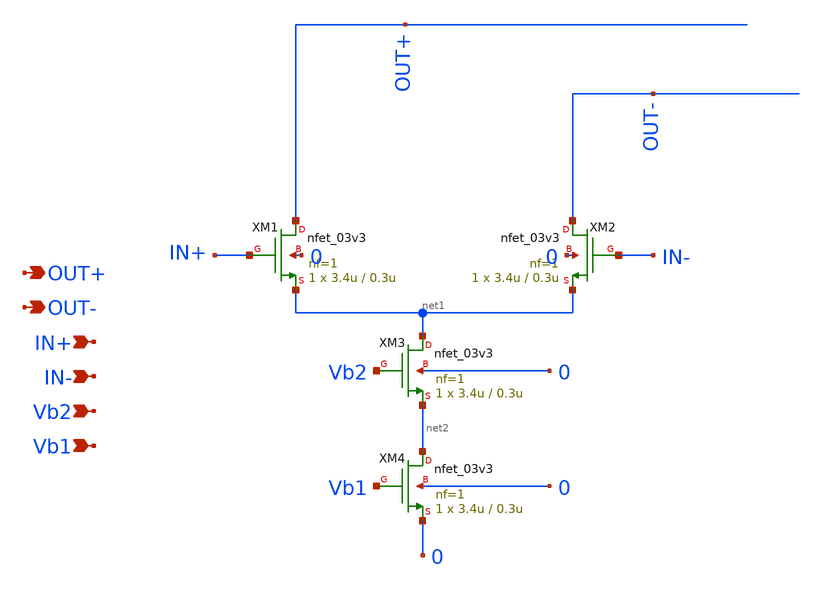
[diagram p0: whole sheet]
** sch_path: initial_notebooks_2023/accepted_notebooks/Current-Steering-DAC/DAC/current_unitx4.sch
**.subckt current_unitx4 IN+ IN- Vb2 Vb1 OUT+ OUT-
*.ipin IN+
*.ipin IN-
*.ipin Vb2
*.ipin Vb1
*.opin OUT+
*.opin OUT-
XM1 OUT+ IN+ net1 0 nfet_03v3 L=0.3u W=3.4u nf=1 ad='int((nf+1)/2) * W/nf * 0.18u' as='int((nf+2)/2) * W/nf * 0.18u'
+ pd='2*int((nf+1)/2) * (W/nf + 0.18u)' ps='2*int((nf+2)/2) * (W/nf + 0.18u)' nrd='0.18u / W' nrs='0.18u / W'
+ sa=0 sb=0 sd=0 m=1
XM2 OUT- IN- net1 0 nfet_03v3 L=0.3u W=3.4u nf=1 ad='int((nf+1)/2) * W/nf * 0.18u' as='int((nf+2)/2) * W/nf * 0.18u'
+ pd='2*int((nf+1)/2) * (W/nf + 0.18u)' ps='2*int((nf+2)/2) * (W/nf + 0.18u)' nrd='0.18u / W' nrs='0.18u / W'
+ sa=0 sb=0 sd=0 m=1
XM3 net1 Vb2 net2 0 nfet_03v3 L=0.3u W=3.4u nf=1 ad='int((nf+1)/2) * W/nf * 0.18u' as='int((nf+2)/2) * W/nf * 0.18u'
+ pd='2*int((nf+1)/2) * (W/nf + 0.18u)' ps='2*int((nf+2)/2) * (W/nf + 0.18u)' nrd='0.18u / W' nrs='0.18u / W'
+ sa=0 sb=0 sd=0 m=1
XM4 net2 Vb1 0 0 nfet_03v3 L=0.3u W=3.4u nf=1 ad='int((nf+1)/2) * W/nf * 0.18u' as='int((nf+2)/2) * W/nf * 0.18u'
+ pd='2*int((nf+1)/2) * (W/nf + 0.18u)' ps='2*int((nf+2)/2) * (W/nf + 0.18u)' nrd='0.18u / W' nrs='0.18u / W'
+ sa=0 sb=0 sd=0 m=1
**.ends
.end
